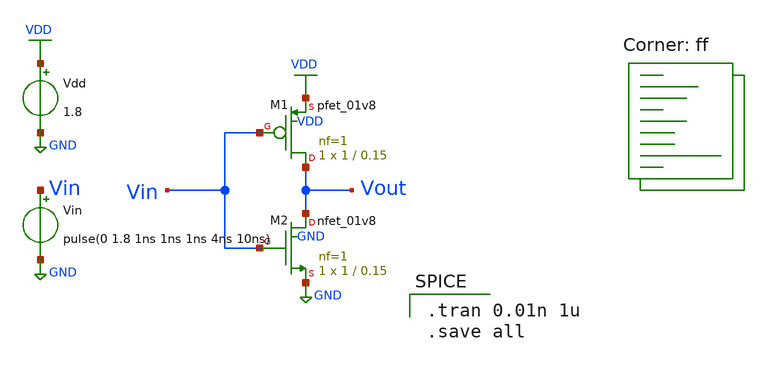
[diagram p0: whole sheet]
** sch_path: MOSFET_analysis/mosfet_analysis_trans.sch
**.subckt mosfet_analysis_trans
XM2 Vout Vin GND GND sky130_fd_pr__nfet_01v8 L=0.15 W=1 nf=1 ad='int((nf+1)/2) * W/nf * 0.29' as='int((nf+2)/2) * W/nf * 0.29'
+ pd='2*int((nf+1)/2) * (W/nf + 0.29)' ps='2*int((nf+2)/2) * (W/nf + 0.29)' nrd='0.29 / W' nrs='0.29 / W'
+ sa=0 sb=0 sd=0 mult=1 m=1
XM1 Vout Vin VDD VDD sky130_fd_pr__pfet_01v8 L=0.15 W=1 nf=1 ad='int((nf+1)/2) * W/nf * 0.29' as='int((nf+2)/2) * W/nf * 0.29'
+ pd='2*int((nf+1)/2) * (W/nf + 0.29)' ps='2*int((nf+2)/2) * (W/nf + 0.29)' nrd='0.29 / W' nrs='0.29 / W'
+ sa=0 sb=0 sd=0 mult=1 m=1
Vdd VDD GND 1.8
Vin Vin GND pulse(0 1.8 1ns 1ns 1ns 4ns 10ns)
**** begin user architecture code

.tran 0.01n 1u
.save all

.lib $::SKYWATER_MODELS/sky130.lib.spice ff
**** end user architecture code
**.ends
.GLOBAL GND
.GLOBAL VDD
.end
